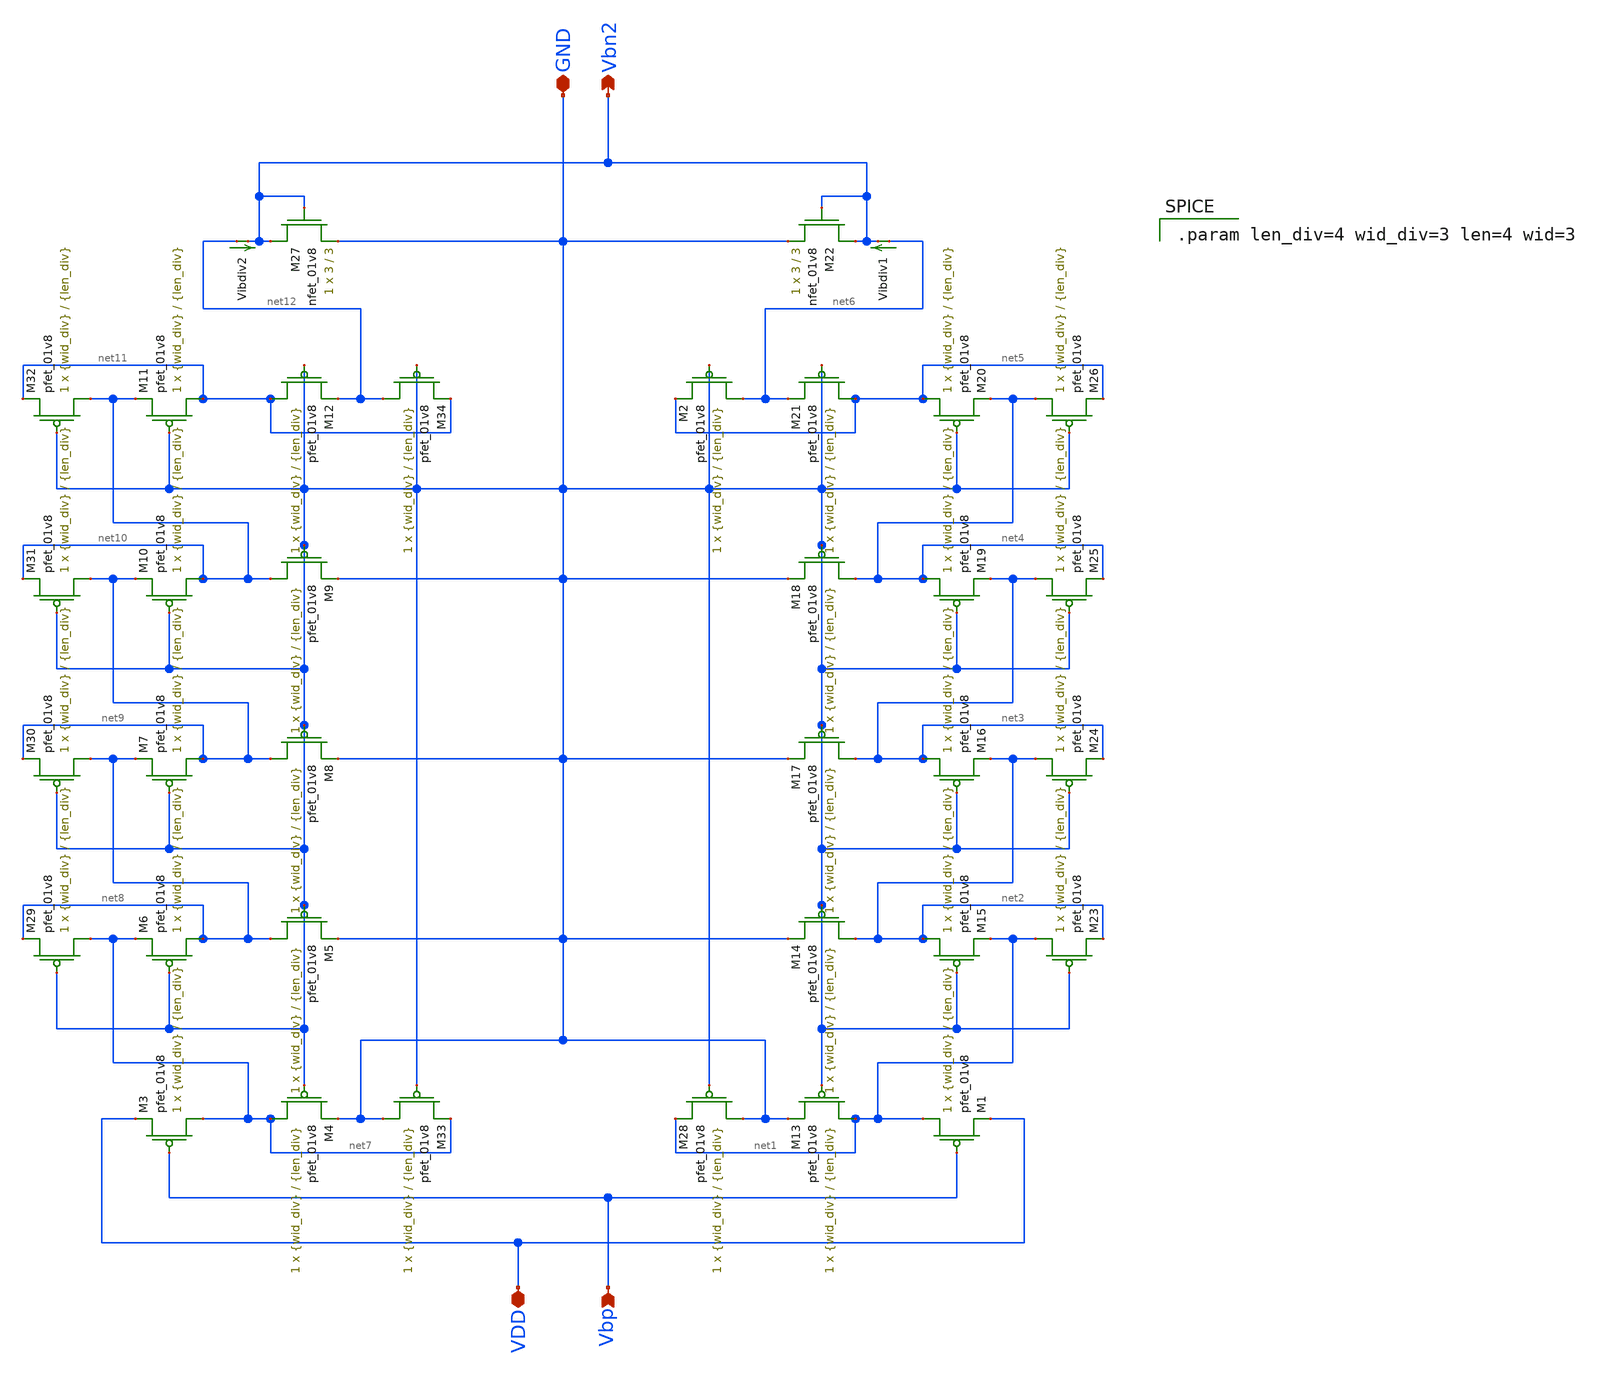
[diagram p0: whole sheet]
** sch_path: mp3/Layout_Schem_Designs/current_divider_lds.sch
**.subckt current_divider_lds GND Vbn2 Vbp VDD
*.iopin GND
*.opin Vbn2
*.ipin Vbp
*.iopin VDD
XM1 net1 Vbp VDD VDD sky130_fd_pr__pfet_01v8 L={len_div} W={wid_div} nf=1 ad='int((nf+1)/2) * W/nf * 0.29'
+ as='int((nf+2)/2) * W/nf * 0.29' pd='2*int((nf+1)/2) * (W/nf + 0.29)' ps='2*int((nf+2)/2) * (W/nf + 0.29)'
+ nrd='0.29 / W' nrs='0.29 / W' sa=0 sb=0 sd=0 mult=1 m=1
XM13 net1 GND GND VDD sky130_fd_pr__pfet_01v8 L={len_div} W={wid_div} nf=1 ad='int((nf+1)/2) * W/nf * 0.29'
+ as='int((nf+2)/2) * W/nf * 0.29' pd='2*int((nf+1)/2) * (W/nf + 0.29)' ps='2*int((nf+2)/2) * (W/nf + 0.29)'
+ nrd='0.29 / W' nrs='0.29 / W' sa=0 sb=0 sd=0 mult=1 m=1
XM14 net2 GND GND VDD sky130_fd_pr__pfet_01v8 L={len_div} W={wid_div} nf=1 ad='int((nf+1)/2) * W/nf * 0.29'
+ as='int((nf+2)/2) * W/nf * 0.29' pd='2*int((nf+1)/2) * (W/nf + 0.29)' ps='2*int((nf+2)/2) * (W/nf + 0.29)'
+ nrd='0.29 / W' nrs='0.29 / W' sa=0 sb=0 sd=0 mult=1 m=1
XM15 net2 GND net1 VDD sky130_fd_pr__pfet_01v8 L={len_div} W={wid_div} nf=1 ad='int((nf+1)/2) * W/nf * 0.29'
+ as='int((nf+2)/2) * W/nf * 0.29' pd='2*int((nf+1)/2) * (W/nf + 0.29)' ps='2*int((nf+2)/2) * (W/nf + 0.29)'
+ nrd='0.29 / W' nrs='0.29 / W' sa=0 sb=0 sd=0 mult=1 m=1
XM16 net3 GND net2 VDD sky130_fd_pr__pfet_01v8 L={len_div} W={wid_div} nf=1 ad='int((nf+1)/2) * W/nf * 0.29'
+ as='int((nf+2)/2) * W/nf * 0.29' pd='2*int((nf+1)/2) * (W/nf + 0.29)' ps='2*int((nf+2)/2) * (W/nf + 0.29)'
+ nrd='0.29 / W' nrs='0.29 / W' sa=0 sb=0 sd=0 mult=1 m=1
XM17 net3 GND GND VDD sky130_fd_pr__pfet_01v8 L={len_div} W={wid_div} nf=1 ad='int((nf+1)/2) * W/nf * 0.29'
+ as='int((nf+2)/2) * W/nf * 0.29' pd='2*int((nf+1)/2) * (W/nf + 0.29)' ps='2*int((nf+2)/2) * (W/nf + 0.29)'
+ nrd='0.29 / W' nrs='0.29 / W' sa=0 sb=0 sd=0 mult=1 m=1
XM18 net4 GND GND VDD sky130_fd_pr__pfet_01v8 L={len_div} W={wid_div} nf=1 ad='int((nf+1)/2) * W/nf * 0.29'
+ as='int((nf+2)/2) * W/nf * 0.29' pd='2*int((nf+1)/2) * (W/nf + 0.29)' ps='2*int((nf+2)/2) * (W/nf + 0.29)'
+ nrd='0.29 / W' nrs='0.29 / W' sa=0 sb=0 sd=0 mult=1 m=1
XM19 net4 GND net3 VDD sky130_fd_pr__pfet_01v8 L={len_div} W={wid_div} nf=1 ad='int((nf+1)/2) * W/nf * 0.29'
+ as='int((nf+2)/2) * W/nf * 0.29' pd='2*int((nf+1)/2) * (W/nf + 0.29)' ps='2*int((nf+2)/2) * (W/nf + 0.29)'
+ nrd='0.29 / W' nrs='0.29 / W' sa=0 sb=0 sd=0 mult=1 m=1
XM20 net5 GND net4 VDD sky130_fd_pr__pfet_01v8 L={len_div} W={wid_div} nf=1 ad='int((nf+1)/2) * W/nf * 0.29'
+ as='int((nf+2)/2) * W/nf * 0.29' pd='2*int((nf+1)/2) * (W/nf + 0.29)' ps='2*int((nf+2)/2) * (W/nf + 0.29)'
+ nrd='0.29 / W' nrs='0.29 / W' sa=0 sb=0 sd=0 mult=1 m=1
XM21 net5 GND net6 VDD sky130_fd_pr__pfet_01v8 L={len_div} W={wid_div} nf=1 ad='int((nf+1)/2) * W/nf * 0.29'
+ as='int((nf+2)/2) * W/nf * 0.29' pd='2*int((nf+1)/2) * (W/nf + 0.29)' ps='2*int((nf+2)/2) * (W/nf + 0.29)'
+ nrd='0.29 / W' nrs='0.29 / W' sa=0 sb=0 sd=0 mult=1 m=1
XM22 Vbn2 Vbn2 GND GND sky130_fd_pr__nfet_01v8 L=3 W=3 nf=1 ad='int((nf+1)/2) * W/nf * 0.29' as='int((nf+2)/2) * W/nf * 0.29'
+ pd='2*int((nf+1)/2) * (W/nf + 0.29)' ps='2*int((nf+2)/2) * (W/nf + 0.29)' nrd='0.29 / W' nrs='0.29 / W'
+ sa=0 sb=0 sd=0 mult=1 m=1
Vibdiv1 net6 Vbn2 0
.save i(vibdiv1)
XM23 net1 GND net2 VDD sky130_fd_pr__pfet_01v8 L={len_div} W={wid_div} nf=1 ad='int((nf+1)/2) * W/nf * 0.29'
+ as='int((nf+2)/2) * W/nf * 0.29' pd='2*int((nf+1)/2) * (W/nf + 0.29)' ps='2*int((nf+2)/2) * (W/nf + 0.29)'
+ nrd='0.29 / W' nrs='0.29 / W' sa=0 sb=0 sd=0 mult=1 m=1
XM24 net2 GND net3 VDD sky130_fd_pr__pfet_01v8 L={len_div} W={wid_div} nf=1 ad='int((nf+1)/2) * W/nf * 0.29'
+ as='int((nf+2)/2) * W/nf * 0.29' pd='2*int((nf+1)/2) * (W/nf + 0.29)' ps='2*int((nf+2)/2) * (W/nf + 0.29)'
+ nrd='0.29 / W' nrs='0.29 / W' sa=0 sb=0 sd=0 mult=1 m=1
XM25 net3 GND net4 VDD sky130_fd_pr__pfet_01v8 L={len_div} W={wid_div} nf=1 ad='int((nf+1)/2) * W/nf * 0.29'
+ as='int((nf+2)/2) * W/nf * 0.29' pd='2*int((nf+1)/2) * (W/nf + 0.29)' ps='2*int((nf+2)/2) * (W/nf + 0.29)'
+ nrd='0.29 / W' nrs='0.29 / W' sa=0 sb=0 sd=0 mult=1 m=1
XM26 net4 GND net5 VDD sky130_fd_pr__pfet_01v8 L={len_div} W={wid_div} nf=1 ad='int((nf+1)/2) * W/nf * 0.29'
+ as='int((nf+2)/2) * W/nf * 0.29' pd='2*int((nf+1)/2) * (W/nf + 0.29)' ps='2*int((nf+2)/2) * (W/nf + 0.29)'
+ nrd='0.29 / W' nrs='0.29 / W' sa=0 sb=0 sd=0 mult=1 m=1
XM28 GND GND net1 VDD sky130_fd_pr__pfet_01v8 L={len_div} W={wid_div} nf=1 ad='int((nf+1)/2) * W/nf * 0.29'
+ as='int((nf+2)/2) * W/nf * 0.29' pd='2*int((nf+1)/2) * (W/nf + 0.29)' ps='2*int((nf+2)/2) * (W/nf + 0.29)'
+ nrd='0.29 / W' nrs='0.29 / W' sa=0 sb=0 sd=0 mult=1 m=1
XM2 net6 GND net5 VDD sky130_fd_pr__pfet_01v8 L={len_div} W={wid_div} nf=1 ad='int((nf+1)/2) * W/nf * 0.29'
+ as='int((nf+2)/2) * W/nf * 0.29' pd='2*int((nf+1)/2) * (W/nf + 0.29)' ps='2*int((nf+2)/2) * (W/nf + 0.29)'
+ nrd='0.29 / W' nrs='0.29 / W' sa=0 sb=0 sd=0 mult=1 m=1
XM3 net7 Vbp VDD VDD sky130_fd_pr__pfet_01v8 L={len_div} W={wid_div} nf=1 ad='int((nf+1)/2) * W/nf * 0.29'
+ as='int((nf+2)/2) * W/nf * 0.29' pd='2*int((nf+1)/2) * (W/nf + 0.29)' ps='2*int((nf+2)/2) * (W/nf + 0.29)'
+ nrd='0.29 / W' nrs='0.29 / W' sa=0 sb=0 sd=0 mult=1 m=1
XM4 net7 GND GND VDD sky130_fd_pr__pfet_01v8 L={len_div} W={wid_div} nf=1 ad='int((nf+1)/2) * W/nf * 0.29'
+ as='int((nf+2)/2) * W/nf * 0.29' pd='2*int((nf+1)/2) * (W/nf + 0.29)' ps='2*int((nf+2)/2) * (W/nf + 0.29)'
+ nrd='0.29 / W' nrs='0.29 / W' sa=0 sb=0 sd=0 mult=1 m=1
XM5 net8 GND GND VDD sky130_fd_pr__pfet_01v8 L={len_div} W={wid_div} nf=1 ad='int((nf+1)/2) * W/nf * 0.29'
+ as='int((nf+2)/2) * W/nf * 0.29' pd='2*int((nf+1)/2) * (W/nf + 0.29)' ps='2*int((nf+2)/2) * (W/nf + 0.29)'
+ nrd='0.29 / W' nrs='0.29 / W' sa=0 sb=0 sd=0 mult=1 m=1
XM6 net8 GND net7 VDD sky130_fd_pr__pfet_01v8 L={len_div} W={wid_div} nf=1 ad='int((nf+1)/2) * W/nf * 0.29'
+ as='int((nf+2)/2) * W/nf * 0.29' pd='2*int((nf+1)/2) * (W/nf + 0.29)' ps='2*int((nf+2)/2) * (W/nf + 0.29)'
+ nrd='0.29 / W' nrs='0.29 / W' sa=0 sb=0 sd=0 mult=1 m=1
XM7 net9 GND net8 VDD sky130_fd_pr__pfet_01v8 L={len_div} W={wid_div} nf=1 ad='int((nf+1)/2) * W/nf * 0.29'
+ as='int((nf+2)/2) * W/nf * 0.29' pd='2*int((nf+1)/2) * (W/nf + 0.29)' ps='2*int((nf+2)/2) * (W/nf + 0.29)'
+ nrd='0.29 / W' nrs='0.29 / W' sa=0 sb=0 sd=0 mult=1 m=1
XM8 net9 GND GND VDD sky130_fd_pr__pfet_01v8 L={len_div} W={wid_div} nf=1 ad='int((nf+1)/2) * W/nf * 0.29'
+ as='int((nf+2)/2) * W/nf * 0.29' pd='2*int((nf+1)/2) * (W/nf + 0.29)' ps='2*int((nf+2)/2) * (W/nf + 0.29)'
+ nrd='0.29 / W' nrs='0.29 / W' sa=0 sb=0 sd=0 mult=1 m=1
XM9 net10 GND GND VDD sky130_fd_pr__pfet_01v8 L={len_div} W={wid_div} nf=1 ad='int((nf+1)/2) * W/nf * 0.29'
+ as='int((nf+2)/2) * W/nf * 0.29' pd='2*int((nf+1)/2) * (W/nf + 0.29)' ps='2*int((nf+2)/2) * (W/nf + 0.29)'
+ nrd='0.29 / W' nrs='0.29 / W' sa=0 sb=0 sd=0 mult=1 m=1
XM10 net10 GND net9 VDD sky130_fd_pr__pfet_01v8 L={len_div} W={wid_div} nf=1 ad='int((nf+1)/2) * W/nf * 0.29'
+ as='int((nf+2)/2) * W/nf * 0.29' pd='2*int((nf+1)/2) * (W/nf + 0.29)' ps='2*int((nf+2)/2) * (W/nf + 0.29)'
+ nrd='0.29 / W' nrs='0.29 / W' sa=0 sb=0 sd=0 mult=1 m=1
XM11 net11 GND net10 VDD sky130_fd_pr__pfet_01v8 L={len_div} W={wid_div} nf=1 ad='int((nf+1)/2) * W/nf * 0.29'
+ as='int((nf+2)/2) * W/nf * 0.29' pd='2*int((nf+1)/2) * (W/nf + 0.29)' ps='2*int((nf+2)/2) * (W/nf + 0.29)'
+ nrd='0.29 / W' nrs='0.29 / W' sa=0 sb=0 sd=0 mult=1 m=1
XM12 net11 GND net12 VDD sky130_fd_pr__pfet_01v8 L={len_div} W={wid_div} nf=1 ad='int((nf+1)/2) * W/nf * 0.29'
+ as='int((nf+2)/2) * W/nf * 0.29' pd='2*int((nf+1)/2) * (W/nf + 0.29)' ps='2*int((nf+2)/2) * (W/nf + 0.29)'
+ nrd='0.29 / W' nrs='0.29 / W' sa=0 sb=0 sd=0 mult=1 m=1
XM27 Vbn2 Vbn2 GND GND sky130_fd_pr__nfet_01v8 L=3 W=3 nf=1 ad='int((nf+1)/2) * W/nf * 0.29' as='int((nf+2)/2) * W/nf * 0.29'
+ pd='2*int((nf+1)/2) * (W/nf + 0.29)' ps='2*int((nf+2)/2) * (W/nf + 0.29)' nrd='0.29 / W' nrs='0.29 / W'
+ sa=0 sb=0 sd=0 mult=1 m=1
Vibdiv2 net12 Vbn2 0
.save i(vibdiv2)
XM29 net7 GND net8 VDD sky130_fd_pr__pfet_01v8 L={len_div} W={wid_div} nf=1 ad='int((nf+1)/2) * W/nf * 0.29'
+ as='int((nf+2)/2) * W/nf * 0.29' pd='2*int((nf+1)/2) * (W/nf + 0.29)' ps='2*int((nf+2)/2) * (W/nf + 0.29)'
+ nrd='0.29 / W' nrs='0.29 / W' sa=0 sb=0 sd=0 mult=1 m=1
XM30 net8 GND net9 VDD sky130_fd_pr__pfet_01v8 L={len_div} W={wid_div} nf=1 ad='int((nf+1)/2) * W/nf * 0.29'
+ as='int((nf+2)/2) * W/nf * 0.29' pd='2*int((nf+1)/2) * (W/nf + 0.29)' ps='2*int((nf+2)/2) * (W/nf + 0.29)'
+ nrd='0.29 / W' nrs='0.29 / W' sa=0 sb=0 sd=0 mult=1 m=1
XM31 net9 GND net10 VDD sky130_fd_pr__pfet_01v8 L={len_div} W={wid_div} nf=1 ad='int((nf+1)/2) * W/nf * 0.29'
+ as='int((nf+2)/2) * W/nf * 0.29' pd='2*int((nf+1)/2) * (W/nf + 0.29)' ps='2*int((nf+2)/2) * (W/nf + 0.29)'
+ nrd='0.29 / W' nrs='0.29 / W' sa=0 sb=0 sd=0 mult=1 m=1
XM32 net10 GND net11 VDD sky130_fd_pr__pfet_01v8 L={len_div} W={wid_div} nf=1 ad='int((nf+1)/2) * W/nf * 0.29'
+ as='int((nf+2)/2) * W/nf * 0.29' pd='2*int((nf+1)/2) * (W/nf + 0.29)' ps='2*int((nf+2)/2) * (W/nf + 0.29)'
+ nrd='0.29 / W' nrs='0.29 / W' sa=0 sb=0 sd=0 mult=1 m=1
XM33 GND GND net7 VDD sky130_fd_pr__pfet_01v8 L={len_div} W={wid_div} nf=1 ad='int((nf+1)/2) * W/nf * 0.29'
+ as='int((nf+2)/2) * W/nf * 0.29' pd='2*int((nf+1)/2) * (W/nf + 0.29)' ps='2*int((nf+2)/2) * (W/nf + 0.29)'
+ nrd='0.29 / W' nrs='0.29 / W' sa=0 sb=0 sd=0 mult=1 m=1
XM34 net12 GND net11 VDD sky130_fd_pr__pfet_01v8 L={len_div} W={wid_div} nf=1 ad='int((nf+1)/2) * W/nf * 0.29'
+ as='int((nf+2)/2) * W/nf * 0.29' pd='2*int((nf+1)/2) * (W/nf + 0.29)' ps='2*int((nf+2)/2) * (W/nf + 0.29)'
+ nrd='0.29 / W' nrs='0.29 / W' sa=0 sb=0 sd=0 mult=1 m=1
**** begin user architecture code

.param len_div=4 wid_div=3 len=4 wid=3

**** end user architecture code
**.ends
.end
